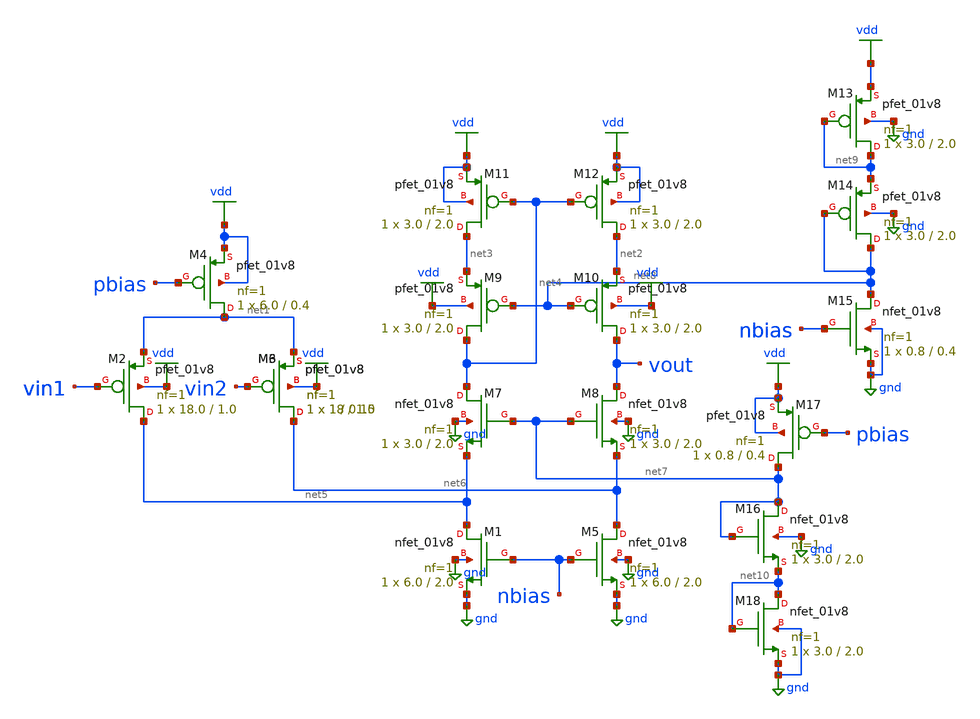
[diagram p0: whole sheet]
** sch_path: project3/fc.sch
**.subckt fc
XM1 net5 nbias gnd gnd sky130_fd_pr__nfet_01v8 L=2.0 W=6.0 nf=1 ad='int((nf+1)/2) * W/nf * 0.29' as='int((nf+2)/2) * W/nf * 0.29'
+ pd='2*int((nf+1)/2) * (W/nf + 0.29)' ps='2*int((nf+2)/2) * (W/nf + 0.29)' nrd='0.29 / W' nrs='0.29 / W'
+ sa=0 sb=0 sd=0 mult=1 m=1
XM2 net5 vin1 net1 vdd sky130_fd_pr__pfet_01v8 L=1.0 W=18.0 nf=1 ad='int((nf+1)/2) * W/nf * 0.29' as='int((nf+2)/2) * W/nf * 0.29'
+ pd='2*int((nf+1)/2) * (W/nf + 0.29)' ps='2*int((nf+2)/2) * (W/nf + 0.29)' nrd='0.29 / W' nrs='0.29 / W'
+ sa=0 sb=0 sd=0 mult=1 m=1
XM3 net6 vin2 net1 vdd sky130_fd_pr__pfet_01v8 L=1.0 W=18 nf=1 ad='int((nf+1)/2) * W/nf * 0.29' as='int((nf+2)/2) * W/nf * 0.29'
+ pd='2*int((nf+1)/2) * (W/nf + 0.29)' ps='2*int((nf+2)/2) * (W/nf + 0.29)' nrd='0.29 / W' nrs='0.29 / W'
+ sa=0 sb=0 sd=0 mult=1 m=1
XM4 net1 pbias vdd vdd sky130_fd_pr__pfet_01v8 L=0.4 W=6.0 nf=1 ad='int((nf+1)/2) * W/nf * 0.29' as='int((nf+2)/2) * W/nf * 0.29'
+ pd='2*int((nf+1)/2) * (W/nf + 0.29)' ps='2*int((nf+2)/2) * (W/nf + 0.29)' nrd='0.29 / W' nrs='0.29 / W'
+ sa=0 sb=0 sd=0 mult=1 m=1
XM5 net6 nbias gnd gnd sky130_fd_pr__nfet_01v8 L=2.0 W=6.0 nf=1 ad='int((nf+1)/2) * W/nf * 0.29' as='int((nf+2)/2) * W/nf * 0.29'
+ pd='2*int((nf+1)/2) * (W/nf + 0.29)' ps='2*int((nf+2)/2) * (W/nf + 0.29)' nrd='0.29 / W' nrs='0.29 / W'
+ sa=0 sb=0 sd=0 mult=1 m=1
XM6 net6 vin2 net1 vdd sky130_fd_pr__pfet_01v8 L=0.15 W=1 nf=1 ad='int((nf+1)/2) * W/nf * 0.29' as='int((nf+2)/2) * W/nf * 0.29'
+ pd='2*int((nf+1)/2) * (W/nf + 0.29)' ps='2*int((nf+2)/2) * (W/nf + 0.29)' nrd='0.29 / W' nrs='0.29 / W'
+ sa=0 sb=0 sd=0 mult=1 m=1
XM7 net4 net7 net5 gnd sky130_fd_pr__nfet_01v8 L=2.0 W=3.0 nf=1 ad='int((nf+1)/2) * W/nf * 0.29' as='int((nf+2)/2) * W/nf * 0.29'
+ pd='2*int((nf+1)/2) * (W/nf + 0.29)' ps='2*int((nf+2)/2) * (W/nf + 0.29)' nrd='0.29 / W' nrs='0.29 / W'
+ sa=0 sb=0 sd=0 mult=1 m=1
XM8 vout net7 net6 gnd sky130_fd_pr__nfet_01v8 L=2.0 W=3.0 nf=1 ad='int((nf+1)/2) * W/nf * 0.29' as='int((nf+2)/2) * W/nf * 0.29'
+ pd='2*int((nf+1)/2) * (W/nf + 0.29)' ps='2*int((nf+2)/2) * (W/nf + 0.29)' nrd='0.29 / W' nrs='0.29 / W'
+ sa=0 sb=0 sd=0 mult=1 m=1
XM9 net4 net8 net3 vdd sky130_fd_pr__pfet_01v8 L=2.0 W=3.0 nf=1 ad='int((nf+1)/2) * W/nf * 0.29' as='int((nf+2)/2) * W/nf * 0.29'
+ pd='2*int((nf+1)/2) * (W/nf + 0.29)' ps='2*int((nf+2)/2) * (W/nf + 0.29)' nrd='0.29 / W' nrs='0.29 / W'
+ sa=0 sb=0 sd=0 mult=1 m=1
XM10 vout net8 net2 vdd sky130_fd_pr__pfet_01v8 L=2.0 W=3.0 nf=1 ad='int((nf+1)/2) * W/nf * 0.29' as='int((nf+2)/2) * W/nf * 0.29'
+ pd='2*int((nf+1)/2) * (W/nf + 0.29)' ps='2*int((nf+2)/2) * (W/nf + 0.29)' nrd='0.29 / W' nrs='0.29 / W'
+ sa=0 sb=0 sd=0 mult=1 m=1
XM11 net3 net4 vdd vdd sky130_fd_pr__pfet_01v8 L=2.0 W=3.0 nf=1 ad='int((nf+1)/2) * W/nf * 0.29' as='int((nf+2)/2) * W/nf * 0.29'
+ pd='2*int((nf+1)/2) * (W/nf + 0.29)' ps='2*int((nf+2)/2) * (W/nf + 0.29)' nrd='0.29 / W' nrs='0.29 / W'
+ sa=0 sb=0 sd=0 mult=1 m=1
XM12 net2 net4 vdd vdd sky130_fd_pr__pfet_01v8 L=2.0 W=3.0 nf=1 ad='int((nf+1)/2) * W/nf * 0.29' as='int((nf+2)/2) * W/nf * 0.29'
+ pd='2*int((nf+1)/2) * (W/nf + 0.29)' ps='2*int((nf+2)/2) * (W/nf + 0.29)' nrd='0.29 / W' nrs='0.29 / W'
+ sa=0 sb=0 sd=0 mult=1 m=1
XM13 net9 net9 vdd gnd sky130_fd_pr__pfet_01v8 L=2.0 W=3.0 nf=1 ad='int((nf+1)/2) * W/nf * 0.29' as='int((nf+2)/2) * W/nf * 0.29'
+ pd='2*int((nf+1)/2) * (W/nf + 0.29)' ps='2*int((nf+2)/2) * (W/nf + 0.29)' nrd='0.29 / W' nrs='0.29 / W'
+ sa=0 sb=0 sd=0 mult=1 m=1
XM14 net8 net8 net9 gnd sky130_fd_pr__pfet_01v8 L=2.0 W=3.0 nf=1 ad='int((nf+1)/2) * W/nf * 0.29' as='int((nf+2)/2) * W/nf * 0.29'
+ pd='2*int((nf+1)/2) * (W/nf + 0.29)' ps='2*int((nf+2)/2) * (W/nf + 0.29)' nrd='0.29 / W' nrs='0.29 / W'
+ sa=0 sb=0 sd=0 mult=1 m=1
XM15 net8 nbias gnd gnd sky130_fd_pr__nfet_01v8 L=0.4 W=0.8 nf=1 ad='int((nf+1)/2) * W/nf * 0.29' as='int((nf+2)/2) * W/nf * 0.29'
+ pd='2*int((nf+1)/2) * (W/nf + 0.29)' ps='2*int((nf+2)/2) * (W/nf + 0.29)' nrd='0.29 / W' nrs='0.29 / W'
+ sa=0 sb=0 sd=0 mult=1 m=1
XM16 net7 net7 net10 gnd sky130_fd_pr__nfet_01v8 L=2.0 W=3.0 nf=1 ad='int((nf+1)/2) * W/nf * 0.29' as='int((nf+2)/2) * W/nf * 0.29'
+ pd='2*int((nf+1)/2) * (W/nf + 0.29)' ps='2*int((nf+2)/2) * (W/nf + 0.29)' nrd='0.29 / W' nrs='0.29 / W'
+ sa=0 sb=0 sd=0 mult=1 m=1
XM17 net7 pbias vdd vdd sky130_fd_pr__pfet_01v8 L=0.4 W=0.8 nf=1 ad='int((nf+1)/2) * W/nf * 0.29' as='int((nf+2)/2) * W/nf * 0.29'
+ pd='2*int((nf+1)/2) * (W/nf + 0.29)' ps='2*int((nf+2)/2) * (W/nf + 0.29)' nrd='0.29 / W' nrs='0.29 / W'
+ sa=0 sb=0 sd=0 mult=1 m=1
XM18 net10 net10 gnd gnd sky130_fd_pr__nfet_01v8 L=2.0 W=3.0 nf=1 ad='int((nf+1)/2) * W/nf * 0.29' as='int((nf+2)/2) * W/nf * 0.29'
+ pd='2*int((nf+1)/2) * (W/nf + 0.29)' ps='2*int((nf+2)/2) * (W/nf + 0.29)' nrd='0.29 / W' nrs='0.29 / W'
+ sa=0 sb=0 sd=0 mult=1 m=1
**.ends
.GLOBAL vdd
.GLOBAL gnd
.end
